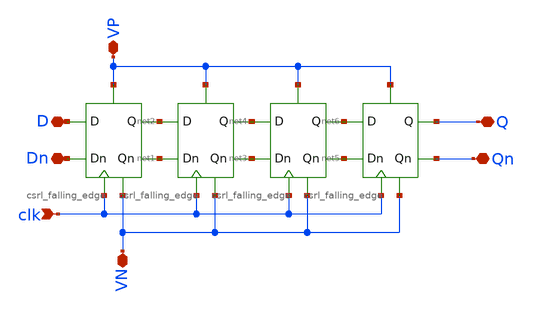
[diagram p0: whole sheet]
** sch_path: lib/digital/schematic/shift_register_x4_falling.sch
**.subckt shift_register_x4_falling clk Q Qn D Dn VP VN
*.ipin clk
*.iopin Q
*.iopin Qn
*.iopin D
*.iopin Dn
*.iopin VP
*.iopin VN
X1 D Dn net1 net2 VN clk VP csrl_falling_edge
X2 net2 net1 net3 net4 VN clk VP csrl_falling_edge
X3 net4 net3 net5 net6 VN clk VP csrl_falling_edge
X4 net6 net5 Qn Q VN clk VP csrl_falling_edge
**.ends
.end
